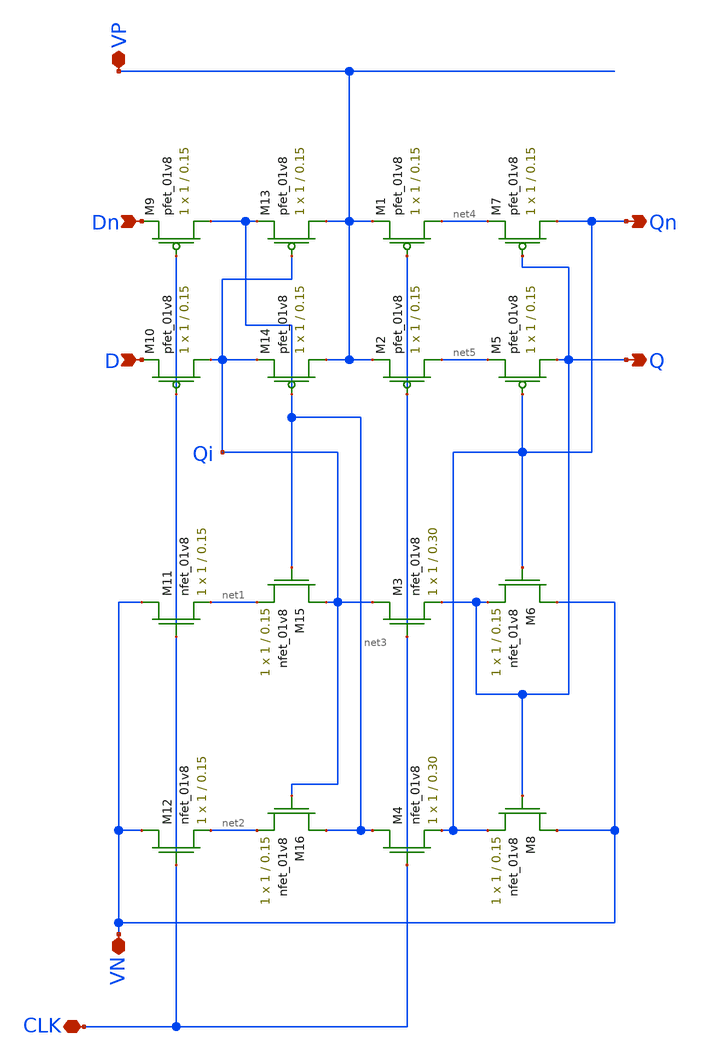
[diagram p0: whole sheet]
** sch_path: schematic/archive/CSRL_D_FF.sch
**.subckt CSRL_D_FF Dn D VP VN CLK Qn Q
*.ipin Dn
*.ipin D
*.iopin VP
*.iopin VN
*.iopin CLK
*.opin Qn
*.opin Q
XM1 net4 CLK VP VDD sky130_fd_pr__pfet_01v8 L=0.15 W=1 nf=1 ad='int((nf+1)/2) * W/nf * 0.29' as='int((nf+2)/2) * W/nf * 0.29'
+ pd='2*int((nf+1)/2) * (W/nf + 0.29)' ps='2*int((nf+2)/2) * (W/nf + 0.29)' nrd='0.29 / W' nrs='0.29 / W'
+ sa=0 sb=0 sd=0 mult=1 m=1
XM2 net5 CLK VP VDD sky130_fd_pr__pfet_01v8 L=0.15 W=1 nf=1 ad='int((nf+1)/2) * W/nf * 0.29' as='int((nf+2)/2) * W/nf * 0.29'
+ pd='2*int((nf+1)/2) * (W/nf + 0.29)' ps='2*int((nf+2)/2) * (W/nf + 0.29)' nrd='0.29 / W' nrs='0.29 / W'
+ sa=0 sb=0 sd=0 mult=1 m=1
XM3 Qi CLK Q GND sky130_fd_pr__nfet_01v8 L=0.30 W=1 nf=1 ad='int((nf+1)/2) * W/nf * 0.29' as='int((nf+2)/2) * W/nf * 0.29'
+ pd='2*int((nf+1)/2) * (W/nf + 0.29)' ps='2*int((nf+2)/2) * (W/nf + 0.29)' nrd='0.29 / W' nrs='0.29 / W'
+ sa=0 sb=0 sd=0 mult=1 m=1
XM4 net3 CLK Qn GND sky130_fd_pr__nfet_01v8 L=0.30 W=1 nf=1 ad='int((nf+1)/2) * W/nf * 0.29' as='int((nf+2)/2) * W/nf * 0.29'
+ pd='2*int((nf+1)/2) * (W/nf + 0.29)' ps='2*int((nf+2)/2) * (W/nf + 0.29)' nrd='0.29 / W' nrs='0.29 / W'
+ sa=0 sb=0 sd=0 mult=1 m=1
XM5 Q Qn net5 VDD sky130_fd_pr__pfet_01v8 L=0.15 W=1 nf=1 ad='int((nf+1)/2) * W/nf * 0.29' as='int((nf+2)/2) * W/nf * 0.29'
+ pd='2*int((nf+1)/2) * (W/nf + 0.29)' ps='2*int((nf+2)/2) * (W/nf + 0.29)' nrd='0.29 / W' nrs='0.29 / W'
+ sa=0 sb=0 sd=0 mult=1 m=1
XM6 VN Qn Q GND sky130_fd_pr__nfet_01v8 L=0.15 W=1 nf=1 ad='int((nf+1)/2) * W/nf * 0.29' as='int((nf+2)/2) * W/nf * 0.29'
+ pd='2*int((nf+1)/2) * (W/nf + 0.29)' ps='2*int((nf+2)/2) * (W/nf + 0.29)' nrd='0.29 / W' nrs='0.29 / W'
+ sa=0 sb=0 sd=0 mult=1 m=1
XM7 Qn Q net4 VDD sky130_fd_pr__pfet_01v8 L=0.15 W=1 nf=1 ad='int((nf+1)/2) * W/nf * 0.29' as='int((nf+2)/2) * W/nf * 0.29'
+ pd='2*int((nf+1)/2) * (W/nf + 0.29)' ps='2*int((nf+2)/2) * (W/nf + 0.29)' nrd='0.29 / W' nrs='0.29 / W'
+ sa=0 sb=0 sd=0 mult=1 m=1
XM8 VN Q Qn GND sky130_fd_pr__nfet_01v8 L=0.15 W=1 nf=1 ad='int((nf+1)/2) * W/nf * 0.29' as='int((nf+2)/2) * W/nf * 0.29'
+ pd='2*int((nf+1)/2) * (W/nf + 0.29)' ps='2*int((nf+2)/2) * (W/nf + 0.29)' nrd='0.29 / W' nrs='0.29 / W'
+ sa=0 sb=0 sd=0 mult=1 m=1
XM9 net3 CLK Dn VDD sky130_fd_pr__pfet_01v8 L=0.15 W=1 nf=1 ad='int((nf+1)/2) * W/nf * 0.29' as='int((nf+2)/2) * W/nf * 0.29'
+ pd='2*int((nf+1)/2) * (W/nf + 0.29)' ps='2*int((nf+2)/2) * (W/nf + 0.29)' nrd='0.29 / W' nrs='0.29 / W'
+ sa=0 sb=0 sd=0 mult=1 m=1
XM10 Qi CLK D VDD sky130_fd_pr__pfet_01v8 L=0.15 W=1 nf=1 ad='int((nf+1)/2) * W/nf * 0.29' as='int((nf+2)/2) * W/nf * 0.29'
+ pd='2*int((nf+1)/2) * (W/nf + 0.29)' ps='2*int((nf+2)/2) * (W/nf + 0.29)' nrd='0.29 / W' nrs='0.29 / W'
+ sa=0 sb=0 sd=0 mult=1 m=1
XM11 VN CLK net1 GND sky130_fd_pr__nfet_01v8 L=0.15 W=1 nf=1 ad='int((nf+1)/2) * W/nf * 0.29' as='int((nf+2)/2) * W/nf * 0.29'
+ pd='2*int((nf+1)/2) * (W/nf + 0.29)' ps='2*int((nf+2)/2) * (W/nf + 0.29)' nrd='0.29 / W' nrs='0.29 / W'
+ sa=0 sb=0 sd=0 mult=1 m=1
XM12 VN CLK net2 GND sky130_fd_pr__nfet_01v8 L=0.15 W=1 nf=1 ad='int((nf+1)/2) * W/nf * 0.29' as='int((nf+2)/2) * W/nf * 0.29'
+ pd='2*int((nf+1)/2) * (W/nf + 0.29)' ps='2*int((nf+2)/2) * (W/nf + 0.29)' nrd='0.29 / W' nrs='0.29 / W'
+ sa=0 sb=0 sd=0 mult=1 m=1
XM13 VP Qi net3 VDD sky130_fd_pr__pfet_01v8 L=0.15 W=1 nf=1 ad='int((nf+1)/2) * W/nf * 0.29' as='int((nf+2)/2) * W/nf * 0.29'
+ pd='2*int((nf+1)/2) * (W/nf + 0.29)' ps='2*int((nf+2)/2) * (W/nf + 0.29)' nrd='0.29 / W' nrs='0.29 / W'
+ sa=0 sb=0 sd=0 mult=1 m=1
XM14 VP net3 Qi VDD sky130_fd_pr__pfet_01v8 L=0.15 W=1 nf=1 ad='int((nf+1)/2) * W/nf * 0.29' as='int((nf+2)/2) * W/nf * 0.29'
+ pd='2*int((nf+1)/2) * (W/nf + 0.29)' ps='2*int((nf+2)/2) * (W/nf + 0.29)' nrd='0.29 / W' nrs='0.29 / W'
+ sa=0 sb=0 sd=0 mult=1 m=1
XM15 Qi net3 net1 GND sky130_fd_pr__nfet_01v8 L=0.15 W=1 nf=1 ad='int((nf+1)/2) * W/nf * 0.29' as='int((nf+2)/2) * W/nf * 0.29'
+ pd='2*int((nf+1)/2) * (W/nf + 0.29)' ps='2*int((nf+2)/2) * (W/nf + 0.29)' nrd='0.29 / W' nrs='0.29 / W'
+ sa=0 sb=0 sd=0 mult=1 m=1
XM16 net3 Qi net2 GND sky130_fd_pr__nfet_01v8 L=0.15 W=1 nf=1 ad='int((nf+1)/2) * W/nf * 0.29' as='int((nf+2)/2) * W/nf * 0.29'
+ pd='2*int((nf+1)/2) * (W/nf + 0.29)' ps='2*int((nf+2)/2) * (W/nf + 0.29)' nrd='0.29 / W' nrs='0.29 / W'
+ sa=0 sb=0 sd=0 mult=1 m=1
**.ends
.end
